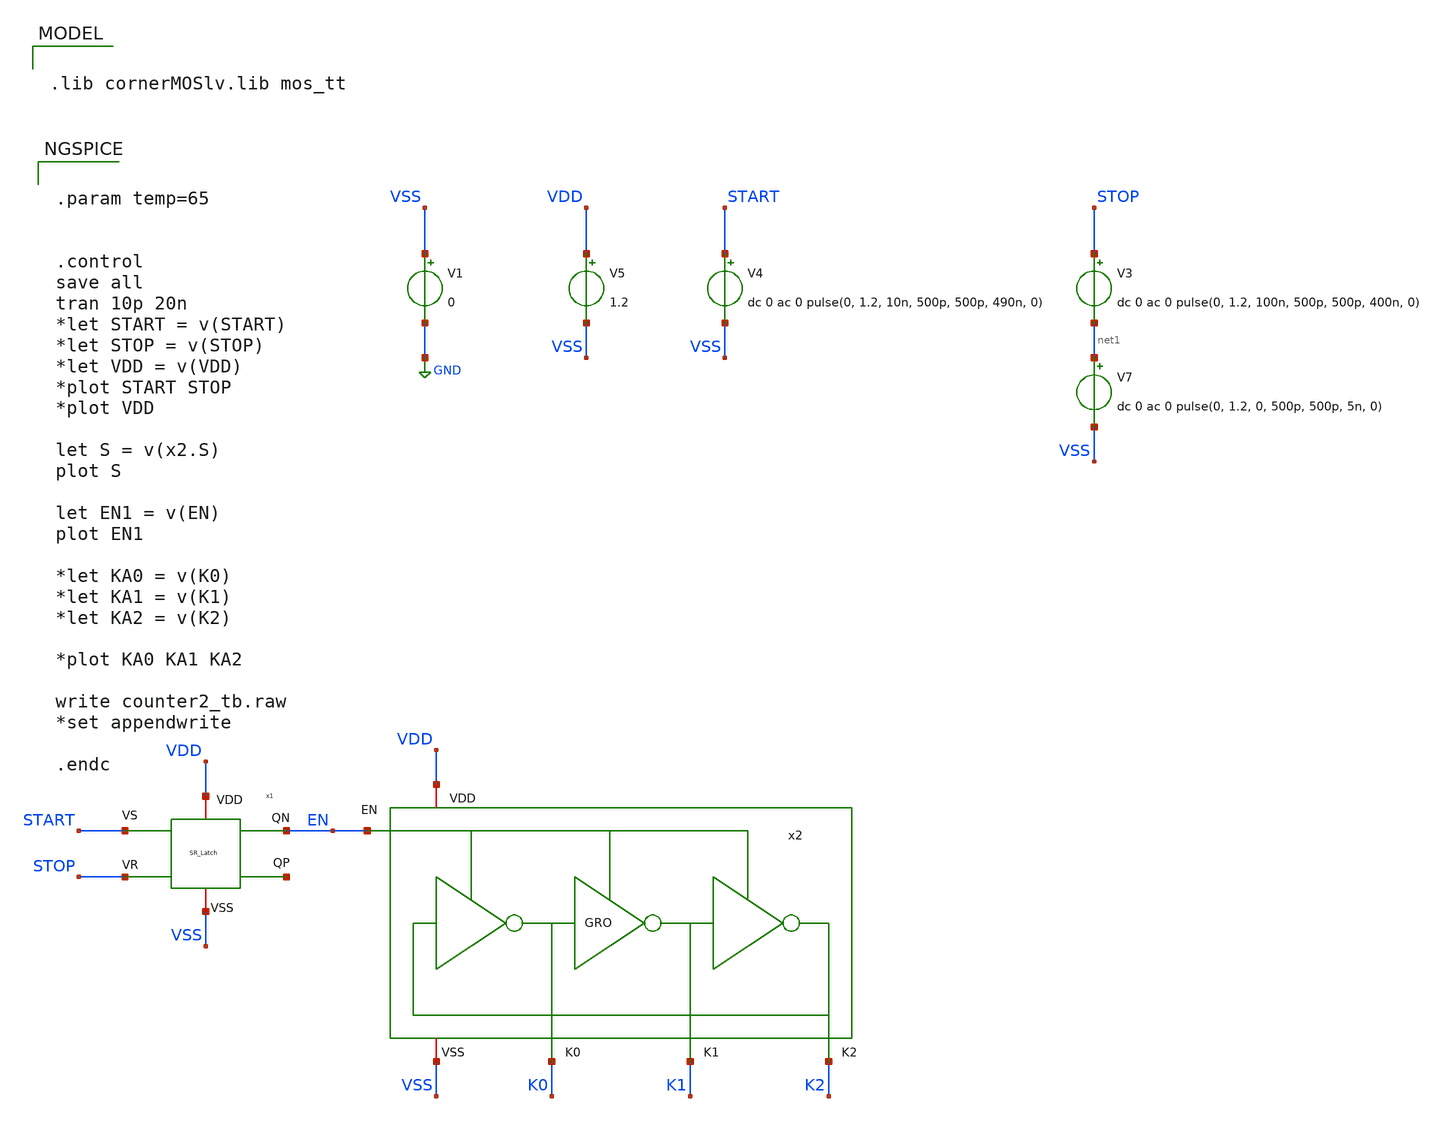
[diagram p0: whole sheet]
** sch_path: ADC8711-main/testbenches/tran/xschem/tb_GRO.sch
**.subckt tb_GRO
V1 VSS GND 0
V3 STOP net1 dc 0 ac 0 pulse(0, 1.2, 100n, 500p, 500p, 400n, 0)
V5 VDD VSS 1.2
V4 START VSS dc 0 ac 0 pulse(0, 1.2, 10n, 500p, 500p, 490n, 0)
V7 net1 VSS dc 0 ac 0 pulse(0, 1.2, 0, 500p, 500p, 5n, 0)
x1 VDD START EN net2 STOP VSS SR_Latch
x2 VDD EN K0 K1 VSS K2 GRO
**** begin user architecture code


.param temp=65


.control
save all
tran 10p 20n
*let START = v(START)
*let STOP = v(STOP)
*let VDD = v(VDD)
*plot START STOP
*plot VDD

let S = v(x2.S)
plot S

let EN1 = v(EN)
plot EN1

*let KA0 = v(K0)
*let KA1 = v(K1)
*let KA2 = v(K2)

*plot KA0 KA1 KA2

write counter2_tb.raw
*set appendwrite

.endc



.lib cornerMOSlv.lib mos_tt

**** end user architecture code
**.ends
.GLOBAL GND
.end
